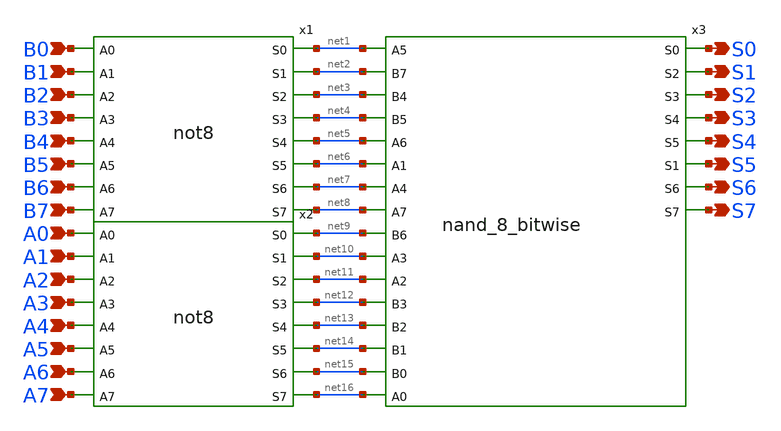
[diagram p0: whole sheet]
** sch_path: design/xschem/OR/OR8.sch
**.subckt OR8 S6 S7 S3 S4 S5 S0 S1 S2 B1 B2 B3 B4 B5 B6 B7 B0 A0 A1 A2 A3 A4 A5 A6 A7
*.opin S6
*.opin S7
*.opin S3
*.opin S4
*.opin S5
*.opin S0
*.opin S1
*.opin S2
*.ipin B1
*.ipin B2
*.ipin B3
*.ipin B4
*.ipin B5
*.ipin B6
*.ipin B7
*.ipin B0
*.ipin A0
*.ipin A1
*.ipin A2
*.ipin A3
*.ipin A4
*.ipin A5
*.ipin A6
*.ipin A7
x1 B0 B1 B2 B3 B4 B5 B6 B7 net1 net2 net3 net4 net5 net6 net7 net8 VSS VDD not8
x2 A0 A1 A2 A3 A4 A5 A6 A7 net9 net10 net11 net12 net13 net14 net15 net16 VSS VDD not8
x3 net1 net2 net3 net4 net5 net6 net7 net8 net9 net10 net11 net12 net13 net14 net15 net16 S0 S1 S2
+ S3 S4 S5 S6 S7 nand_8_bitwise
**.ends
.end
